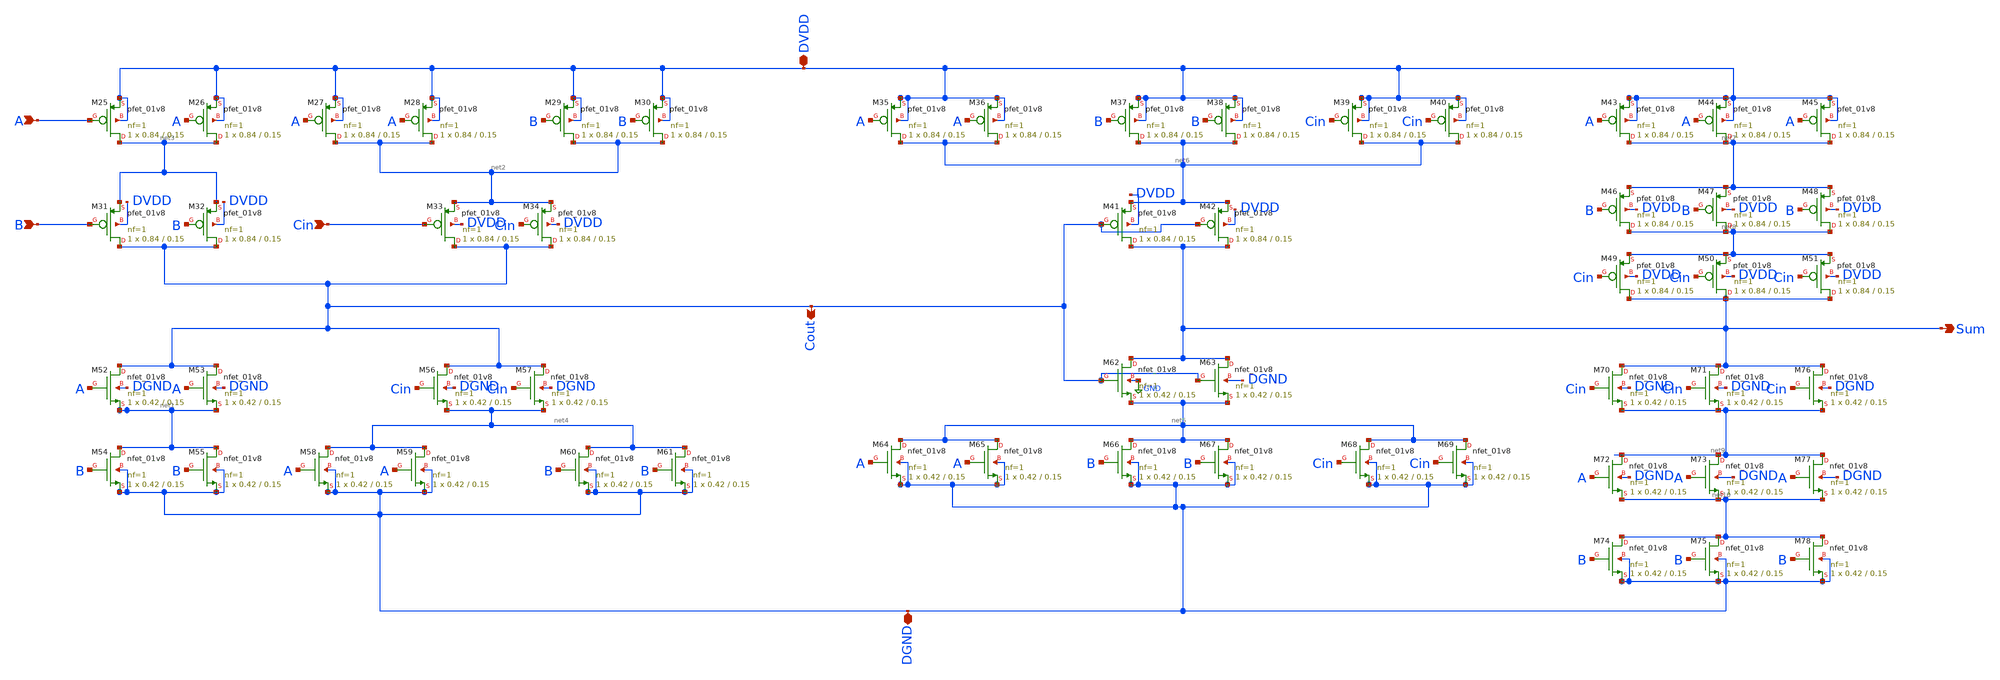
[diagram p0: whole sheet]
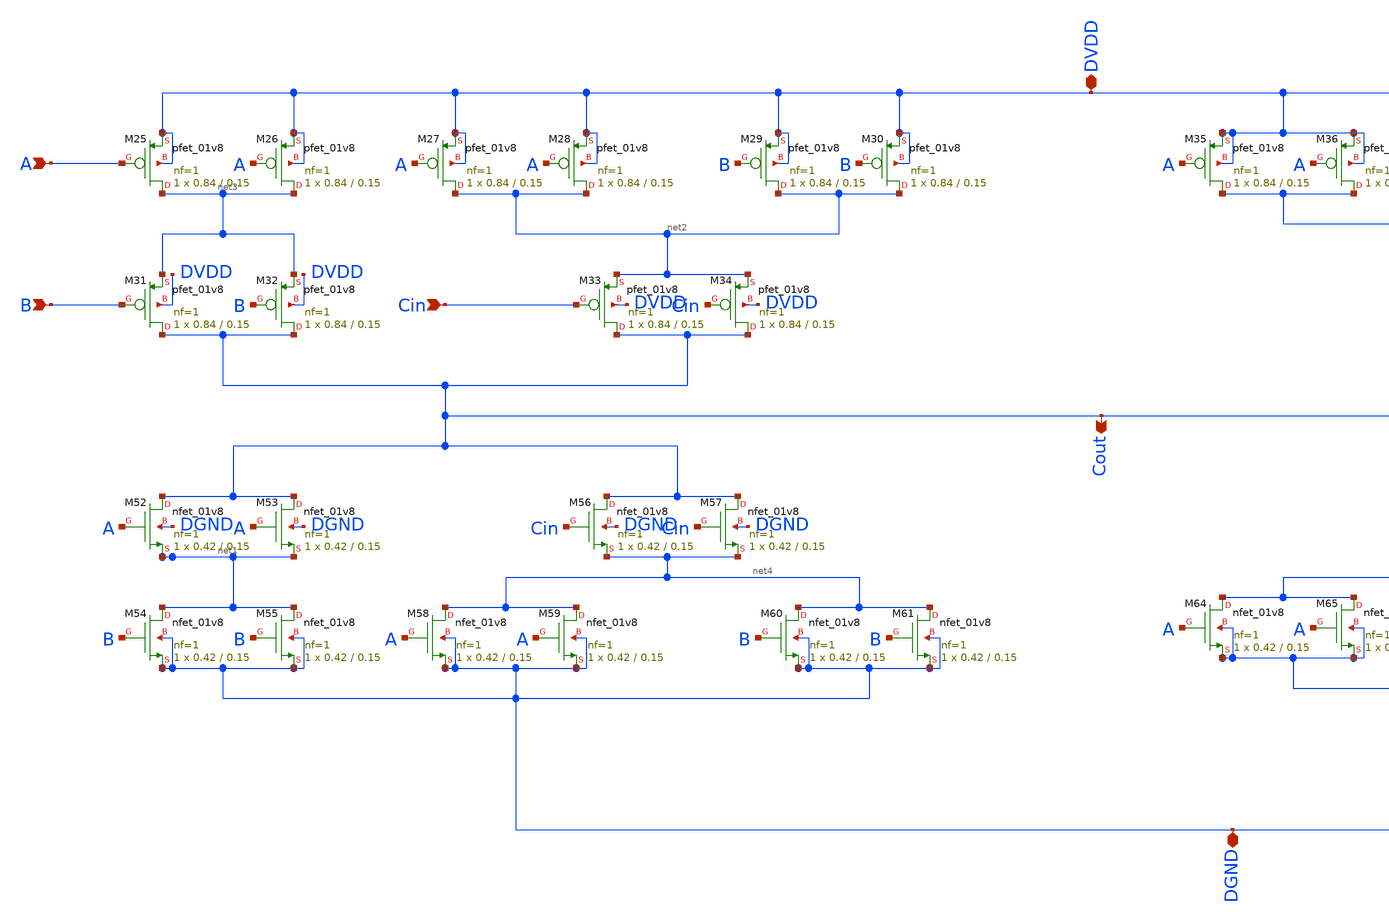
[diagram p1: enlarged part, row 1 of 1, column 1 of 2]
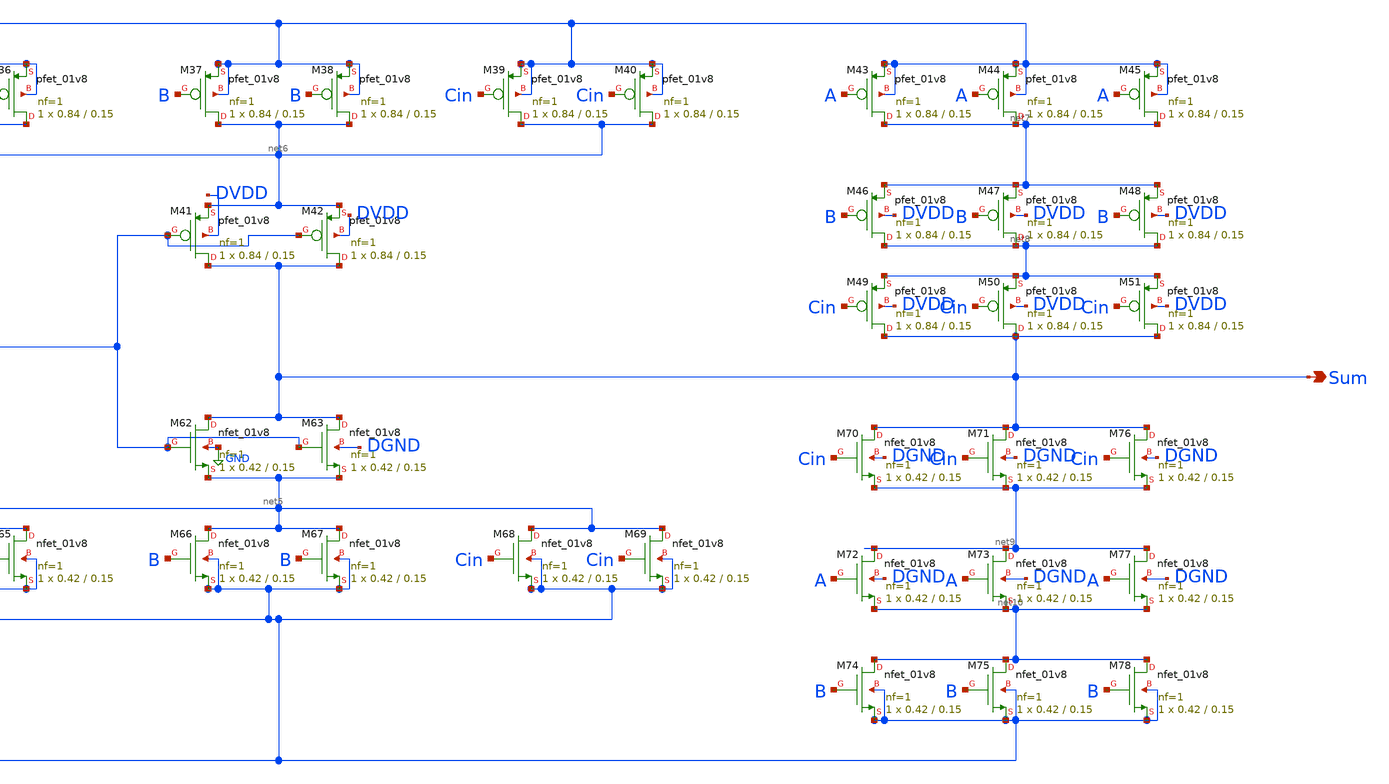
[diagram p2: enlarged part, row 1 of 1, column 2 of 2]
** sch_path: Tutorial_6/Part-B/fulladder.sch
**.subckt fulladder Cout Sum A B Cin DVDD DGND
*.opin Cout
*.opin Sum
*.ipin A
*.ipin B
*.ipin Cin
*.iopin DVDD
*.iopin DGND
XM25 net3 A DVDD DVDD sky130_fd_pr__pfet_01v8 L=0.15 W=0.84 nf=1 ad='int((nf+1)/2) * W/nf * 0.29' as='int((nf+2)/2) * W/nf * 0.29'
+ pd='2*int((nf+1)/2) * (W/nf + 0.29)' ps='2*int((nf+2)/2) * (W/nf + 0.29)' nrd='0.29 / W' nrs='0.29 / W'
+ sa=0 sb=0 sd=0 mult=1 m=1
XM26 net3 A DVDD DVDD sky130_fd_pr__pfet_01v8 L=0.15 W=0.84 nf=1 ad='int((nf+1)/2) * W/nf * 0.29' as='int((nf+2)/2) * W/nf * 0.29'
+ pd='2*int((nf+1)/2) * (W/nf + 0.29)' ps='2*int((nf+2)/2) * (W/nf + 0.29)' nrd='0.29 / W' nrs='0.29 / W'
+ sa=0 sb=0 sd=0 mult=1 m=1
XM27 net2 A DVDD DVDD sky130_fd_pr__pfet_01v8 L=0.15 W=0.84 nf=1 ad='int((nf+1)/2) * W/nf * 0.29' as='int((nf+2)/2) * W/nf * 0.29'
+ pd='2*int((nf+1)/2) * (W/nf + 0.29)' ps='2*int((nf+2)/2) * (W/nf + 0.29)' nrd='0.29 / W' nrs='0.29 / W'
+ sa=0 sb=0 sd=0 mult=1 m=1
XM28 net2 A DVDD DVDD sky130_fd_pr__pfet_01v8 L=0.15 W=0.84 nf=1 ad='int((nf+1)/2) * W/nf * 0.29' as='int((nf+2)/2) * W/nf * 0.29'
+ pd='2*int((nf+1)/2) * (W/nf + 0.29)' ps='2*int((nf+2)/2) * (W/nf + 0.29)' nrd='0.29 / W' nrs='0.29 / W'
+ sa=0 sb=0 sd=0 mult=1 m=1
XM29 net2 B DVDD DVDD sky130_fd_pr__pfet_01v8 L=0.15 W=0.84 nf=1 ad='int((nf+1)/2) * W/nf * 0.29' as='int((nf+2)/2) * W/nf * 0.29'
+ pd='2*int((nf+1)/2) * (W/nf + 0.29)' ps='2*int((nf+2)/2) * (W/nf + 0.29)' nrd='0.29 / W' nrs='0.29 / W'
+ sa=0 sb=0 sd=0 mult=1 m=1
XM30 net2 B DVDD DVDD sky130_fd_pr__pfet_01v8 L=0.15 W=0.84 nf=1 ad='int((nf+1)/2) * W/nf * 0.29' as='int((nf+2)/2) * W/nf * 0.29'
+ pd='2*int((nf+1)/2) * (W/nf + 0.29)' ps='2*int((nf+2)/2) * (W/nf + 0.29)' nrd='0.29 / W' nrs='0.29 / W'
+ sa=0 sb=0 sd=0 mult=1 m=1
XM31 Cout B net3 DVDD sky130_fd_pr__pfet_01v8 L=0.15 W=0.84 nf=1 ad='int((nf+1)/2) * W/nf * 0.29' as='int((nf+2)/2) * W/nf * 0.29'
+ pd='2*int((nf+1)/2) * (W/nf + 0.29)' ps='2*int((nf+2)/2) * (W/nf + 0.29)' nrd='0.29 / W' nrs='0.29 / W'
+ sa=0 sb=0 sd=0 mult=1 m=1
XM32 Cout B net3 DVDD sky130_fd_pr__pfet_01v8 L=0.15 W=0.84 nf=1 ad='int((nf+1)/2) * W/nf * 0.29' as='int((nf+2)/2) * W/nf * 0.29'
+ pd='2*int((nf+1)/2) * (W/nf + 0.29)' ps='2*int((nf+2)/2) * (W/nf + 0.29)' nrd='0.29 / W' nrs='0.29 / W'
+ sa=0 sb=0 sd=0 mult=1 m=1
XM33 Cout Cin net2 DVDD sky130_fd_pr__pfet_01v8 L=0.15 W=0.84 nf=1 ad='int((nf+1)/2) * W/nf * 0.29' as='int((nf+2)/2) * W/nf * 0.29'
+ pd='2*int((nf+1)/2) * (W/nf + 0.29)' ps='2*int((nf+2)/2) * (W/nf + 0.29)' nrd='0.29 / W' nrs='0.29 / W'
+ sa=0 sb=0 sd=0 mult=1 m=1
XM34 Cout Cin net2 DVDD sky130_fd_pr__pfet_01v8 L=0.15 W=0.84 nf=1 ad='int((nf+1)/2) * W/nf * 0.29' as='int((nf+2)/2) * W/nf * 0.29'
+ pd='2*int((nf+1)/2) * (W/nf + 0.29)' ps='2*int((nf+2)/2) * (W/nf + 0.29)' nrd='0.29 / W' nrs='0.29 / W'
+ sa=0 sb=0 sd=0 mult=1 m=1
XM35 net6 A DVDD DVDD sky130_fd_pr__pfet_01v8 L=0.15 W=0.84 nf=1 ad='int((nf+1)/2) * W/nf * 0.29' as='int((nf+2)/2) * W/nf * 0.29'
+ pd='2*int((nf+1)/2) * (W/nf + 0.29)' ps='2*int((nf+2)/2) * (W/nf + 0.29)' nrd='0.29 / W' nrs='0.29 / W'
+ sa=0 sb=0 sd=0 mult=1 m=1
XM36 net6 A DVDD DVDD sky130_fd_pr__pfet_01v8 L=0.15 W=0.84 nf=1 ad='int((nf+1)/2) * W/nf * 0.29' as='int((nf+2)/2) * W/nf * 0.29'
+ pd='2*int((nf+1)/2) * (W/nf + 0.29)' ps='2*int((nf+2)/2) * (W/nf + 0.29)' nrd='0.29 / W' nrs='0.29 / W'
+ sa=0 sb=0 sd=0 mult=1 m=1
XM37 net6 B DVDD DVDD sky130_fd_pr__pfet_01v8 L=0.15 W=0.84 nf=1 ad='int((nf+1)/2) * W/nf * 0.29' as='int((nf+2)/2) * W/nf * 0.29'
+ pd='2*int((nf+1)/2) * (W/nf + 0.29)' ps='2*int((nf+2)/2) * (W/nf + 0.29)' nrd='0.29 / W' nrs='0.29 / W'
+ sa=0 sb=0 sd=0 mult=1 m=1
XM38 net6 B DVDD DVDD sky130_fd_pr__pfet_01v8 L=0.15 W=0.84 nf=1 ad='int((nf+1)/2) * W/nf * 0.29' as='int((nf+2)/2) * W/nf * 0.29'
+ pd='2*int((nf+1)/2) * (W/nf + 0.29)' ps='2*int((nf+2)/2) * (W/nf + 0.29)' nrd='0.29 / W' nrs='0.29 / W'
+ sa=0 sb=0 sd=0 mult=1 m=1
XM39 net6 Cin DVDD DVDD sky130_fd_pr__pfet_01v8 L=0.15 W=0.84 nf=1 ad='int((nf+1)/2) * W/nf * 0.29' as='int((nf+2)/2) * W/nf * 0.29'
+ pd='2*int((nf+1)/2) * (W/nf + 0.29)' ps='2*int((nf+2)/2) * (W/nf + 0.29)' nrd='0.29 / W' nrs='0.29 / W'
+ sa=0 sb=0 sd=0 mult=1 m=1
XM40 net6 Cin DVDD DVDD sky130_fd_pr__pfet_01v8 L=0.15 W=0.84 nf=1 ad='int((nf+1)/2) * W/nf * 0.29' as='int((nf+2)/2) * W/nf * 0.29'
+ pd='2*int((nf+1)/2) * (W/nf + 0.29)' ps='2*int((nf+2)/2) * (W/nf + 0.29)' nrd='0.29 / W' nrs='0.29 / W'
+ sa=0 sb=0 sd=0 mult=1 m=1
XM41 Sum Cout net6 DVDD sky130_fd_pr__pfet_01v8 L=0.15 W=0.84 nf=1 ad='int((nf+1)/2) * W/nf * 0.29' as='int((nf+2)/2) * W/nf * 0.29'
+ pd='2*int((nf+1)/2) * (W/nf + 0.29)' ps='2*int((nf+2)/2) * (W/nf + 0.29)' nrd='0.29 / W' nrs='0.29 / W'
+ sa=0 sb=0 sd=0 mult=1 m=1
XM42 Sum Cout net6 DVDD sky130_fd_pr__pfet_01v8 L=0.15 W=0.84 nf=1 ad='int((nf+1)/2) * W/nf * 0.29' as='int((nf+2)/2) * W/nf * 0.29'
+ pd='2*int((nf+1)/2) * (W/nf + 0.29)' ps='2*int((nf+2)/2) * (W/nf + 0.29)' nrd='0.29 / W' nrs='0.29 / W'
+ sa=0 sb=0 sd=0 mult=1 m=1
XM43 net7 A DVDD DVDD sky130_fd_pr__pfet_01v8 L=0.15 W=0.84 nf=1 ad='int((nf+1)/2) * W/nf * 0.29' as='int((nf+2)/2) * W/nf * 0.29'
+ pd='2*int((nf+1)/2) * (W/nf + 0.29)' ps='2*int((nf+2)/2) * (W/nf + 0.29)' nrd='0.29 / W' nrs='0.29 / W'
+ sa=0 sb=0 sd=0 mult=1 m=1
XM44 net7 A DVDD DVDD sky130_fd_pr__pfet_01v8 L=0.15 W=0.84 nf=1 ad='int((nf+1)/2) * W/nf * 0.29' as='int((nf+2)/2) * W/nf * 0.29'
+ pd='2*int((nf+1)/2) * (W/nf + 0.29)' ps='2*int((nf+2)/2) * (W/nf + 0.29)' nrd='0.29 / W' nrs='0.29 / W'
+ sa=0 sb=0 sd=0 mult=1 m=1
XM45 net7 A DVDD DVDD sky130_fd_pr__pfet_01v8 L=0.15 W=0.84 nf=1 ad='int((nf+1)/2) * W/nf * 0.29' as='int((nf+2)/2) * W/nf * 0.29'
+ pd='2*int((nf+1)/2) * (W/nf + 0.29)' ps='2*int((nf+2)/2) * (W/nf + 0.29)' nrd='0.29 / W' nrs='0.29 / W'
+ sa=0 sb=0 sd=0 mult=1 m=1
XM46 net8 B net7 DVDD sky130_fd_pr__pfet_01v8 L=0.15 W=0.84 nf=1 ad='int((nf+1)/2) * W/nf * 0.29' as='int((nf+2)/2) * W/nf * 0.29'
+ pd='2*int((nf+1)/2) * (W/nf + 0.29)' ps='2*int((nf+2)/2) * (W/nf + 0.29)' nrd='0.29 / W' nrs='0.29 / W'
+ sa=0 sb=0 sd=0 mult=1 m=1
XM47 net8 B net7 DVDD sky130_fd_pr__pfet_01v8 L=0.15 W=0.84 nf=1 ad='int((nf+1)/2) * W/nf * 0.29' as='int((nf+2)/2) * W/nf * 0.29'
+ pd='2*int((nf+1)/2) * (W/nf + 0.29)' ps='2*int((nf+2)/2) * (W/nf + 0.29)' nrd='0.29 / W' nrs='0.29 / W'
+ sa=0 sb=0 sd=0 mult=1 m=1
XM48 net8 B net7 DVDD sky130_fd_pr__pfet_01v8 L=0.15 W=0.84 nf=1 ad='int((nf+1)/2) * W/nf * 0.29' as='int((nf+2)/2) * W/nf * 0.29'
+ pd='2*int((nf+1)/2) * (W/nf + 0.29)' ps='2*int((nf+2)/2) * (W/nf + 0.29)' nrd='0.29 / W' nrs='0.29 / W'
+ sa=0 sb=0 sd=0 mult=1 m=1
XM49 Sum Cin net8 DVDD sky130_fd_pr__pfet_01v8 L=0.15 W=0.84 nf=1 ad='int((nf+1)/2) * W/nf * 0.29' as='int((nf+2)/2) * W/nf * 0.29'
+ pd='2*int((nf+1)/2) * (W/nf + 0.29)' ps='2*int((nf+2)/2) * (W/nf + 0.29)' nrd='0.29 / W' nrs='0.29 / W'
+ sa=0 sb=0 sd=0 mult=1 m=1
XM50 Sum Cin net8 DVDD sky130_fd_pr__pfet_01v8 L=0.15 W=0.84 nf=1 ad='int((nf+1)/2) * W/nf * 0.29' as='int((nf+2)/2) * W/nf * 0.29'
+ pd='2*int((nf+1)/2) * (W/nf + 0.29)' ps='2*int((nf+2)/2) * (W/nf + 0.29)' nrd='0.29 / W' nrs='0.29 / W'
+ sa=0 sb=0 sd=0 mult=1 m=1
XM51 Sum Cin net8 DVDD sky130_fd_pr__pfet_01v8 L=0.15 W=0.84 nf=1 ad='int((nf+1)/2) * W/nf * 0.29' as='int((nf+2)/2) * W/nf * 0.29'
+ pd='2*int((nf+1)/2) * (W/nf + 0.29)' ps='2*int((nf+2)/2) * (W/nf + 0.29)' nrd='0.29 / W' nrs='0.29 / W'
+ sa=0 sb=0 sd=0 mult=1 m=1
XM52 Cout A net1 DGND sky130_fd_pr__nfet_01v8 L=0.15 W=0.42 nf=1 ad='int((nf+1)/2) * W/nf * 0.29' as='int((nf+2)/2) * W/nf * 0.29'
+ pd='2*int((nf+1)/2) * (W/nf + 0.29)' ps='2*int((nf+2)/2) * (W/nf + 0.29)' nrd='0.29 / W' nrs='0.29 / W'
+ sa=0 sb=0 sd=0 mult=1 m=1
XM53 Cout A net1 DGND sky130_fd_pr__nfet_01v8 L=0.15 W=0.42 nf=1 ad='int((nf+1)/2) * W/nf * 0.29' as='int((nf+2)/2) * W/nf * 0.29'
+ pd='2*int((nf+1)/2) * (W/nf + 0.29)' ps='2*int((nf+2)/2) * (W/nf + 0.29)' nrd='0.29 / W' nrs='0.29 / W'
+ sa=0 sb=0 sd=0 mult=1 m=1
XM54 net1 B DGND DGND sky130_fd_pr__nfet_01v8 L=0.15 W=0.42 nf=1 ad='int((nf+1)/2) * W/nf * 0.29' as='int((nf+2)/2) * W/nf * 0.29'
+ pd='2*int((nf+1)/2) * (W/nf + 0.29)' ps='2*int((nf+2)/2) * (W/nf + 0.29)' nrd='0.29 / W' nrs='0.29 / W'
+ sa=0 sb=0 sd=0 mult=1 m=1
XM55 net1 B DGND DGND sky130_fd_pr__nfet_01v8 L=0.15 W=0.42 nf=1 ad='int((nf+1)/2) * W/nf * 0.29' as='int((nf+2)/2) * W/nf * 0.29'
+ pd='2*int((nf+1)/2) * (W/nf + 0.29)' ps='2*int((nf+2)/2) * (W/nf + 0.29)' nrd='0.29 / W' nrs='0.29 / W'
+ sa=0 sb=0 sd=0 mult=1 m=1
XM56 Cout Cin net4 DGND sky130_fd_pr__nfet_01v8 L=0.15 W=0.42 nf=1 ad='int((nf+1)/2) * W/nf * 0.29' as='int((nf+2)/2) * W/nf * 0.29'
+ pd='2*int((nf+1)/2) * (W/nf + 0.29)' ps='2*int((nf+2)/2) * (W/nf + 0.29)' nrd='0.29 / W' nrs='0.29 / W'
+ sa=0 sb=0 sd=0 mult=1 m=1
XM57 Cout Cin net4 DGND sky130_fd_pr__nfet_01v8 L=0.15 W=0.42 nf=1 ad='int((nf+1)/2) * W/nf * 0.29' as='int((nf+2)/2) * W/nf * 0.29'
+ pd='2*int((nf+1)/2) * (W/nf + 0.29)' ps='2*int((nf+2)/2) * (W/nf + 0.29)' nrd='0.29 / W' nrs='0.29 / W'
+ sa=0 sb=0 sd=0 mult=1 m=1
XM58 net4 A DGND DGND sky130_fd_pr__nfet_01v8 L=0.15 W=0.42 nf=1 ad='int((nf+1)/2) * W/nf * 0.29' as='int((nf+2)/2) * W/nf * 0.29'
+ pd='2*int((nf+1)/2) * (W/nf + 0.29)' ps='2*int((nf+2)/2) * (W/nf + 0.29)' nrd='0.29 / W' nrs='0.29 / W'
+ sa=0 sb=0 sd=0 mult=1 m=1
XM59 net4 A DGND DGND sky130_fd_pr__nfet_01v8 L=0.15 W=0.42 nf=1 ad='int((nf+1)/2) * W/nf * 0.29' as='int((nf+2)/2) * W/nf * 0.29'
+ pd='2*int((nf+1)/2) * (W/nf + 0.29)' ps='2*int((nf+2)/2) * (W/nf + 0.29)' nrd='0.29 / W' nrs='0.29 / W'
+ sa=0 sb=0 sd=0 mult=1 m=1
XM60 net4 B DGND DGND sky130_fd_pr__nfet_01v8 L=0.15 W=0.42 nf=1 ad='int((nf+1)/2) * W/nf * 0.29' as='int((nf+2)/2) * W/nf * 0.29'
+ pd='2*int((nf+1)/2) * (W/nf + 0.29)' ps='2*int((nf+2)/2) * (W/nf + 0.29)' nrd='0.29 / W' nrs='0.29 / W'
+ sa=0 sb=0 sd=0 mult=1 m=1
XM61 net4 B DGND DGND sky130_fd_pr__nfet_01v8 L=0.15 W=0.42 nf=1 ad='int((nf+1)/2) * W/nf * 0.29' as='int((nf+2)/2) * W/nf * 0.29'
+ pd='2*int((nf+1)/2) * (W/nf + 0.29)' ps='2*int((nf+2)/2) * (W/nf + 0.29)' nrd='0.29 / W' nrs='0.29 / W'
+ sa=0 sb=0 sd=0 mult=1 m=1
XM62 Sum Cout net5 GND sky130_fd_pr__nfet_01v8 L=0.15 W=0.42 nf=1 ad='int((nf+1)/2) * W/nf * 0.29' as='int((nf+2)/2) * W/nf * 0.29'
+ pd='2*int((nf+1)/2) * (W/nf + 0.29)' ps='2*int((nf+2)/2) * (W/nf + 0.29)' nrd='0.29 / W' nrs='0.29 / W'
+ sa=0 sb=0 sd=0 mult=1 m=1
XM63 Sum Cout net5 DGND sky130_fd_pr__nfet_01v8 L=0.15 W=0.42 nf=1 ad='int((nf+1)/2) * W/nf * 0.29' as='int((nf+2)/2) * W/nf * 0.29'
+ pd='2*int((nf+1)/2) * (W/nf + 0.29)' ps='2*int((nf+2)/2) * (W/nf + 0.29)' nrd='0.29 / W' nrs='0.29 / W'
+ sa=0 sb=0 sd=0 mult=1 m=1
XM64 net5 A DGND DGND sky130_fd_pr__nfet_01v8 L=0.15 W=0.42 nf=1 ad='int((nf+1)/2) * W/nf * 0.29' as='int((nf+2)/2) * W/nf * 0.29'
+ pd='2*int((nf+1)/2) * (W/nf + 0.29)' ps='2*int((nf+2)/2) * (W/nf + 0.29)' nrd='0.29 / W' nrs='0.29 / W'
+ sa=0 sb=0 sd=0 mult=1 m=1
XM65 net5 A DGND DGND sky130_fd_pr__nfet_01v8 L=0.15 W=0.42 nf=1 ad='int((nf+1)/2) * W/nf * 0.29' as='int((nf+2)/2) * W/nf * 0.29'
+ pd='2*int((nf+1)/2) * (W/nf + 0.29)' ps='2*int((nf+2)/2) * (W/nf + 0.29)' nrd='0.29 / W' nrs='0.29 / W'
+ sa=0 sb=0 sd=0 mult=1 m=1
XM66 net5 B DGND DGND sky130_fd_pr__nfet_01v8 L=0.15 W=0.42 nf=1 ad='int((nf+1)/2) * W/nf * 0.29' as='int((nf+2)/2) * W/nf * 0.29'
+ pd='2*int((nf+1)/2) * (W/nf + 0.29)' ps='2*int((nf+2)/2) * (W/nf + 0.29)' nrd='0.29 / W' nrs='0.29 / W'
+ sa=0 sb=0 sd=0 mult=1 m=1
XM67 net5 B DGND DGND sky130_fd_pr__nfet_01v8 L=0.15 W=0.42 nf=1 ad='int((nf+1)/2) * W/nf * 0.29' as='int((nf+2)/2) * W/nf * 0.29'
+ pd='2*int((nf+1)/2) * (W/nf + 0.29)' ps='2*int((nf+2)/2) * (W/nf + 0.29)' nrd='0.29 / W' nrs='0.29 / W'
+ sa=0 sb=0 sd=0 mult=1 m=1
XM68 net5 Cin DGND DGND sky130_fd_pr__nfet_01v8 L=0.15 W=0.42 nf=1 ad='int((nf+1)/2) * W/nf * 0.29' as='int((nf+2)/2) * W/nf * 0.29'
+ pd='2*int((nf+1)/2) * (W/nf + 0.29)' ps='2*int((nf+2)/2) * (W/nf + 0.29)' nrd='0.29 / W' nrs='0.29 / W'
+ sa=0 sb=0 sd=0 mult=1 m=1
XM69 net5 Cin DGND DGND sky130_fd_pr__nfet_01v8 L=0.15 W=0.42 nf=1 ad='int((nf+1)/2) * W/nf * 0.29' as='int((nf+2)/2) * W/nf * 0.29'
+ pd='2*int((nf+1)/2) * (W/nf + 0.29)' ps='2*int((nf+2)/2) * (W/nf + 0.29)' nrd='0.29 / W' nrs='0.29 / W'
+ sa=0 sb=0 sd=0 mult=1 m=1
XM70 Sum Cin net9 DGND sky130_fd_pr__nfet_01v8 L=0.15 W=0.42 nf=1 ad='int((nf+1)/2) * W/nf * 0.29' as='int((nf+2)/2) * W/nf * 0.29'
+ pd='2*int((nf+1)/2) * (W/nf + 0.29)' ps='2*int((nf+2)/2) * (W/nf + 0.29)' nrd='0.29 / W' nrs='0.29 / W'
+ sa=0 sb=0 sd=0 mult=1 m=1
XM71 Sum Cin net9 DGND sky130_fd_pr__nfet_01v8 L=0.15 W=0.42 nf=1 ad='int((nf+1)/2) * W/nf * 0.29' as='int((nf+2)/2) * W/nf * 0.29'
+ pd='2*int((nf+1)/2) * (W/nf + 0.29)' ps='2*int((nf+2)/2) * (W/nf + 0.29)' nrd='0.29 / W' nrs='0.29 / W'
+ sa=0 sb=0 sd=0 mult=1 m=1
XM72 net9 A net10 DGND sky130_fd_pr__nfet_01v8 L=0.15 W=0.42 nf=1 ad='int((nf+1)/2) * W/nf * 0.29' as='int((nf+2)/2) * W/nf * 0.29'
+ pd='2*int((nf+1)/2) * (W/nf + 0.29)' ps='2*int((nf+2)/2) * (W/nf + 0.29)' nrd='0.29 / W' nrs='0.29 / W'
+ sa=0 sb=0 sd=0 mult=1 m=1
XM73 net9 A net10 DGND sky130_fd_pr__nfet_01v8 L=0.15 W=0.42 nf=1 ad='int((nf+1)/2) * W/nf * 0.29' as='int((nf+2)/2) * W/nf * 0.29'
+ pd='2*int((nf+1)/2) * (W/nf + 0.29)' ps='2*int((nf+2)/2) * (W/nf + 0.29)' nrd='0.29 / W' nrs='0.29 / W'
+ sa=0 sb=0 sd=0 mult=1 m=1
XM74 net10 B DGND DGND sky130_fd_pr__nfet_01v8 L=0.15 W=0.42 nf=1 ad='int((nf+1)/2) * W/nf * 0.29' as='int((nf+2)/2) * W/nf * 0.29'
+ pd='2*int((nf+1)/2) * (W/nf + 0.29)' ps='2*int((nf+2)/2) * (W/nf + 0.29)' nrd='0.29 / W' nrs='0.29 / W'
+ sa=0 sb=0 sd=0 mult=1 m=1
XM75 net10 B DGND DGND sky130_fd_pr__nfet_01v8 L=0.15 W=0.42 nf=1 ad='int((nf+1)/2) * W/nf * 0.29' as='int((nf+2)/2) * W/nf * 0.29'
+ pd='2*int((nf+1)/2) * (W/nf + 0.29)' ps='2*int((nf+2)/2) * (W/nf + 0.29)' nrd='0.29 / W' nrs='0.29 / W'
+ sa=0 sb=0 sd=0 mult=1 m=1
XM76 Sum Cin net9 DGND sky130_fd_pr__nfet_01v8 L=0.15 W=0.42 nf=1 ad='int((nf+1)/2) * W/nf * 0.29' as='int((nf+2)/2) * W/nf * 0.29'
+ pd='2*int((nf+1)/2) * (W/nf + 0.29)' ps='2*int((nf+2)/2) * (W/nf + 0.29)' nrd='0.29 / W' nrs='0.29 / W'
+ sa=0 sb=0 sd=0 mult=1 m=1
XM77 net9 A net10 DGND sky130_fd_pr__nfet_01v8 L=0.15 W=0.42 nf=1 ad='int((nf+1)/2) * W/nf * 0.29' as='int((nf+2)/2) * W/nf * 0.29'
+ pd='2*int((nf+1)/2) * (W/nf + 0.29)' ps='2*int((nf+2)/2) * (W/nf + 0.29)' nrd='0.29 / W' nrs='0.29 / W'
+ sa=0 sb=0 sd=0 mult=1 m=1
XM78 net10 B DGND DGND sky130_fd_pr__nfet_01v8 L=0.15 W=0.42 nf=1 ad='int((nf+1)/2) * W/nf * 0.29' as='int((nf+2)/2) * W/nf * 0.29'
+ pd='2*int((nf+1)/2) * (W/nf + 0.29)' ps='2*int((nf+2)/2) * (W/nf + 0.29)' nrd='0.29 / W' nrs='0.29 / W'
+ sa=0 sb=0 sd=0 mult=1 m=1
**.ends
.GLOBAL GND
.end
